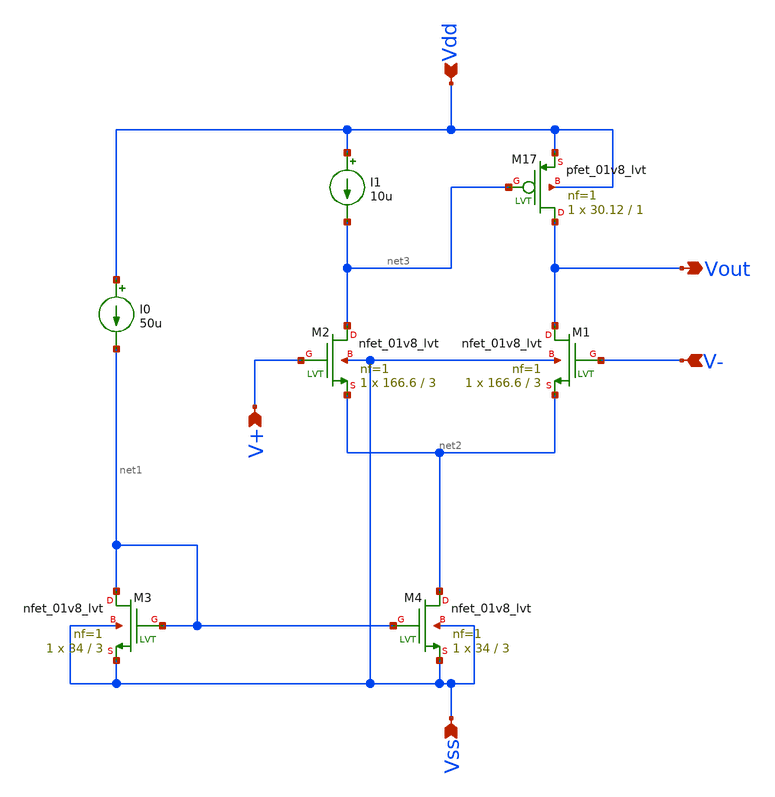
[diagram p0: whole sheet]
** sch_path: xschem/MY_OTA.sch
**.subckt MY_OTA Vout Vdd Vss V+ V-
*.opin Vout
*.ipin Vdd
*.ipin Vss
*.ipin V+
*.ipin V-
I0 Vdd net1 50u
I1 Vdd net3 10u
XM17 Vout net3 Vdd Vdd sky130_fd_pr__pfet_01v8_lvt L=1 W=30.12 nf=1 ad='int((1 + 1)/2) * 30.12 / 1 * 0.29'
+ as='int((1 + 2)/2) * 30.12 / 1 * 0.29' pd='2*int((1 + 1)/2) * (30.12 / 1 + 0.29)' ps='2*int((1 + 2)/2) * (30.12 / 1 + 0.29)'
+ nrd='0.29 / 30.12 ' nrs='0.29 / 30.12 ' sa=0 sb=0 sd=0 mult=1 m=1
XM2 net3 V+ net2 Vss sky130_fd_pr__nfet_01v8_lvt L=3 W=166.6 nf=1 ad='int((1 + 1)/2) * 166.6 / 1 * 0.29'
+ as='int((1 + 2)/2) * 166.6 / 1 * 0.29' pd='2*int((1 + 1)/2) * (166.6 / 1 + 0.29)' ps='2*int((1 + 2)/2) * (166.6 / 1 + 0.29)'
+ nrd='0.29 / 166.6 ' nrs='0.29 / 166.6 ' sa=0 sb=0 sd=0 mult=1 m=1
XM1 Vout V- net2 Vss sky130_fd_pr__nfet_01v8_lvt L=3 W=166.6 nf=1 ad='int((1 + 1)/2) * 166.6 / 1 * 0.29'
+ as='int((1 + 2)/2) * 166.6 / 1 * 0.29' pd='2*int((1 + 1)/2) * (166.6 / 1 + 0.29)' ps='2*int((1 + 2)/2) * (166.6 / 1 + 0.29)'
+ nrd='0.29 / 166.6 ' nrs='0.29 / 166.6 ' sa=0 sb=0 sd=0 mult=1 m=1
XM3 net1 net1 Vss Vss sky130_fd_pr__nfet_01v8_lvt L=3 W=34 nf=1 ad='int((1 + 1)/2) * 34 / 1 * 0.29' as='int((1 + 2)/2) * 34 / 1 * 0.29'
+ pd='2*int((1 + 1)/2) * (34 / 1 + 0.29)' ps='2*int((1 + 2)/2) * (34 / 1 + 0.29)' nrd='0.29 / 34 ' nrs='0.29 / 34 '
+ sa=0 sb=0 sd=0 mult=1 m=1
XM4 net2 net1 Vss Vss sky130_fd_pr__nfet_01v8_lvt L=3 W=34 nf=1 ad='int((1 + 1)/2) * 34 / 1 * 0.29' as='int((1 + 2)/2) * 34 / 1 * 0.29'
+ pd='2*int((1 + 1)/2) * (34 / 1 + 0.29)' ps='2*int((1 + 2)/2) * (34 / 1 + 0.29)' nrd='0.29 / 34 ' nrs='0.29 / 34 '
+ sa=0 sb=0 sd=0 mult=1 m=1
**.ends
.end
